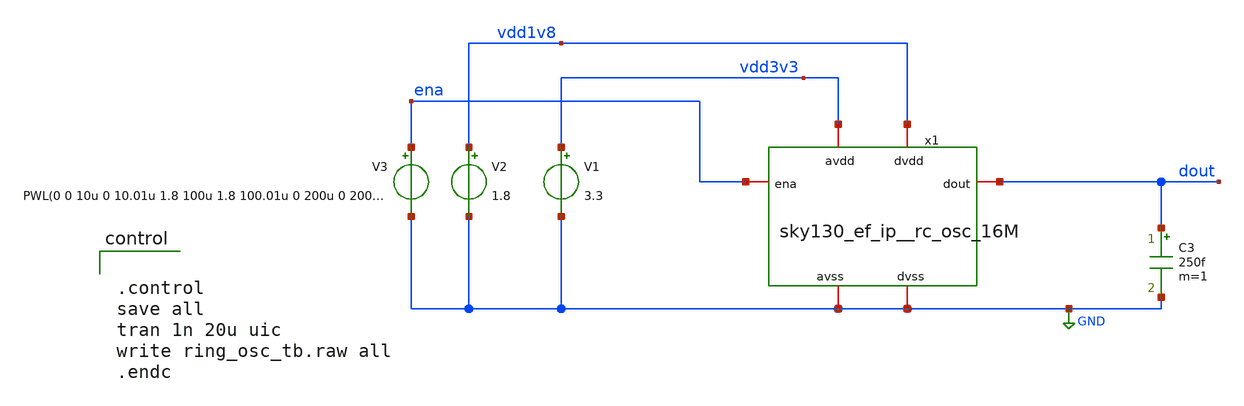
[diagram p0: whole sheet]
** sch_path: cace/templates/ring_osc_tb.sch
**.subckt ring_osc_tb
x1 ena vdd1v8 vdd3v3 GND GND dout sky130_ef_ip__rc_osc_16M
V1 vdd3v3 GND 3.3
V2 vdd1v8 GND 1.8
C3 dout GND 250f m=1
V3 ena GND PWL(0 0 10u 0 10.01u 1.8 100u 1.8 100.01u 0 200u 0 200.01u 1.8)
**** begin user architecture code


.lib /usr/share/pdk/sky130A/libs.tech/ngspice/sky130.lib.spice tt




.control
save all
tran 1n 20u uic
write ring_osc_tb.raw all
.endc


**** end user architecture code
**.ends
.GLOBAL GND
.end
